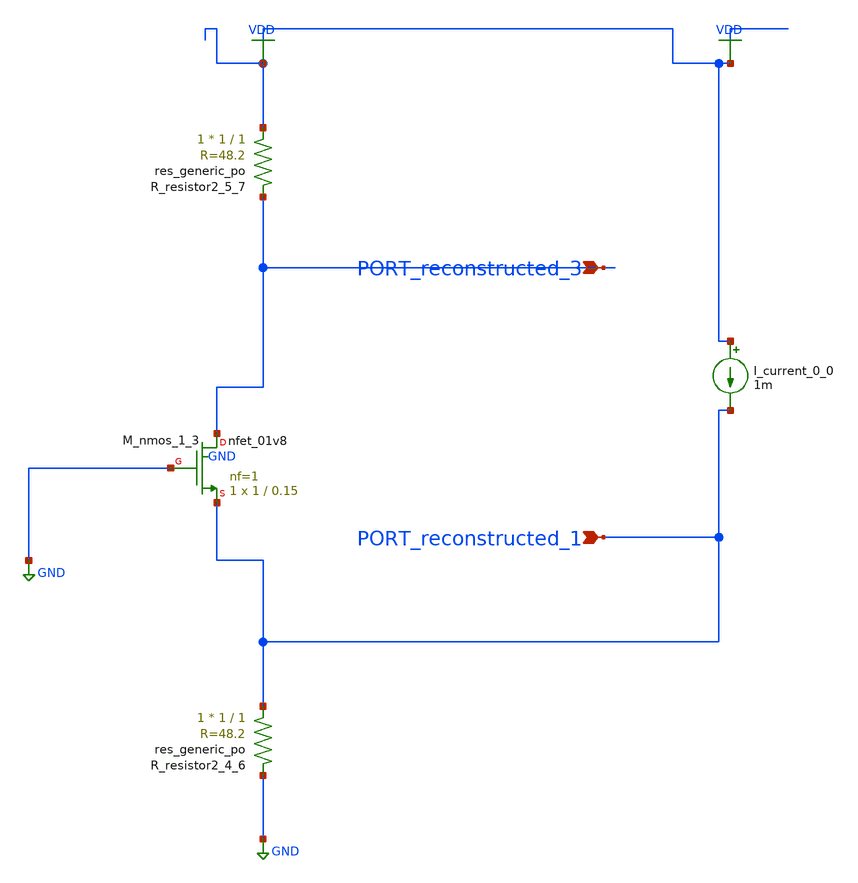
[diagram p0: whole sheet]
** sch_path: schematics/AMSNet/594.sch
**.subckt 594 PORT_reconstructed_1 PORT_reconstructed_3
*.ipin PORT_reconstructed_1
*.ipin PORT_reconstructed_3
I_current_0_0 VDD PORT_reconstructed_1 1m
XM_nmos_1_3 PORT_reconstructed_3 GND PORT_reconstructed_1 GND sky130_fd_pr__nfet_01v8 L=0.15 W=1 nf=1
+ ad='int((1 + 1)/2) * 1 / 1 * 0.29' as='int((1 + 2)/2) * 1 / 1 * 0.29' pd='2*int((1 + 1)/2) * (1 / 1 + 0.29)'
+ ps='2*int((1 + 2)/2) * (1 / 1 + 0.29)' nrd='0.29 / 1 ' nrs='0.29 / 1 ' sa=0 sb=0 sd=0 mult=1 m=1
XR_resistor2_4_6 PORT_reconstructed_1 GND sky130_fd_pr__res_generic_po W=1 L=1 m=1
XR_resistor2_5_7 VDD PORT_reconstructed_3 sky130_fd_pr__res_generic_po W=1 L=1 m=1
**.ends
.GLOBAL GND
.GLOBAL VDD
.end
